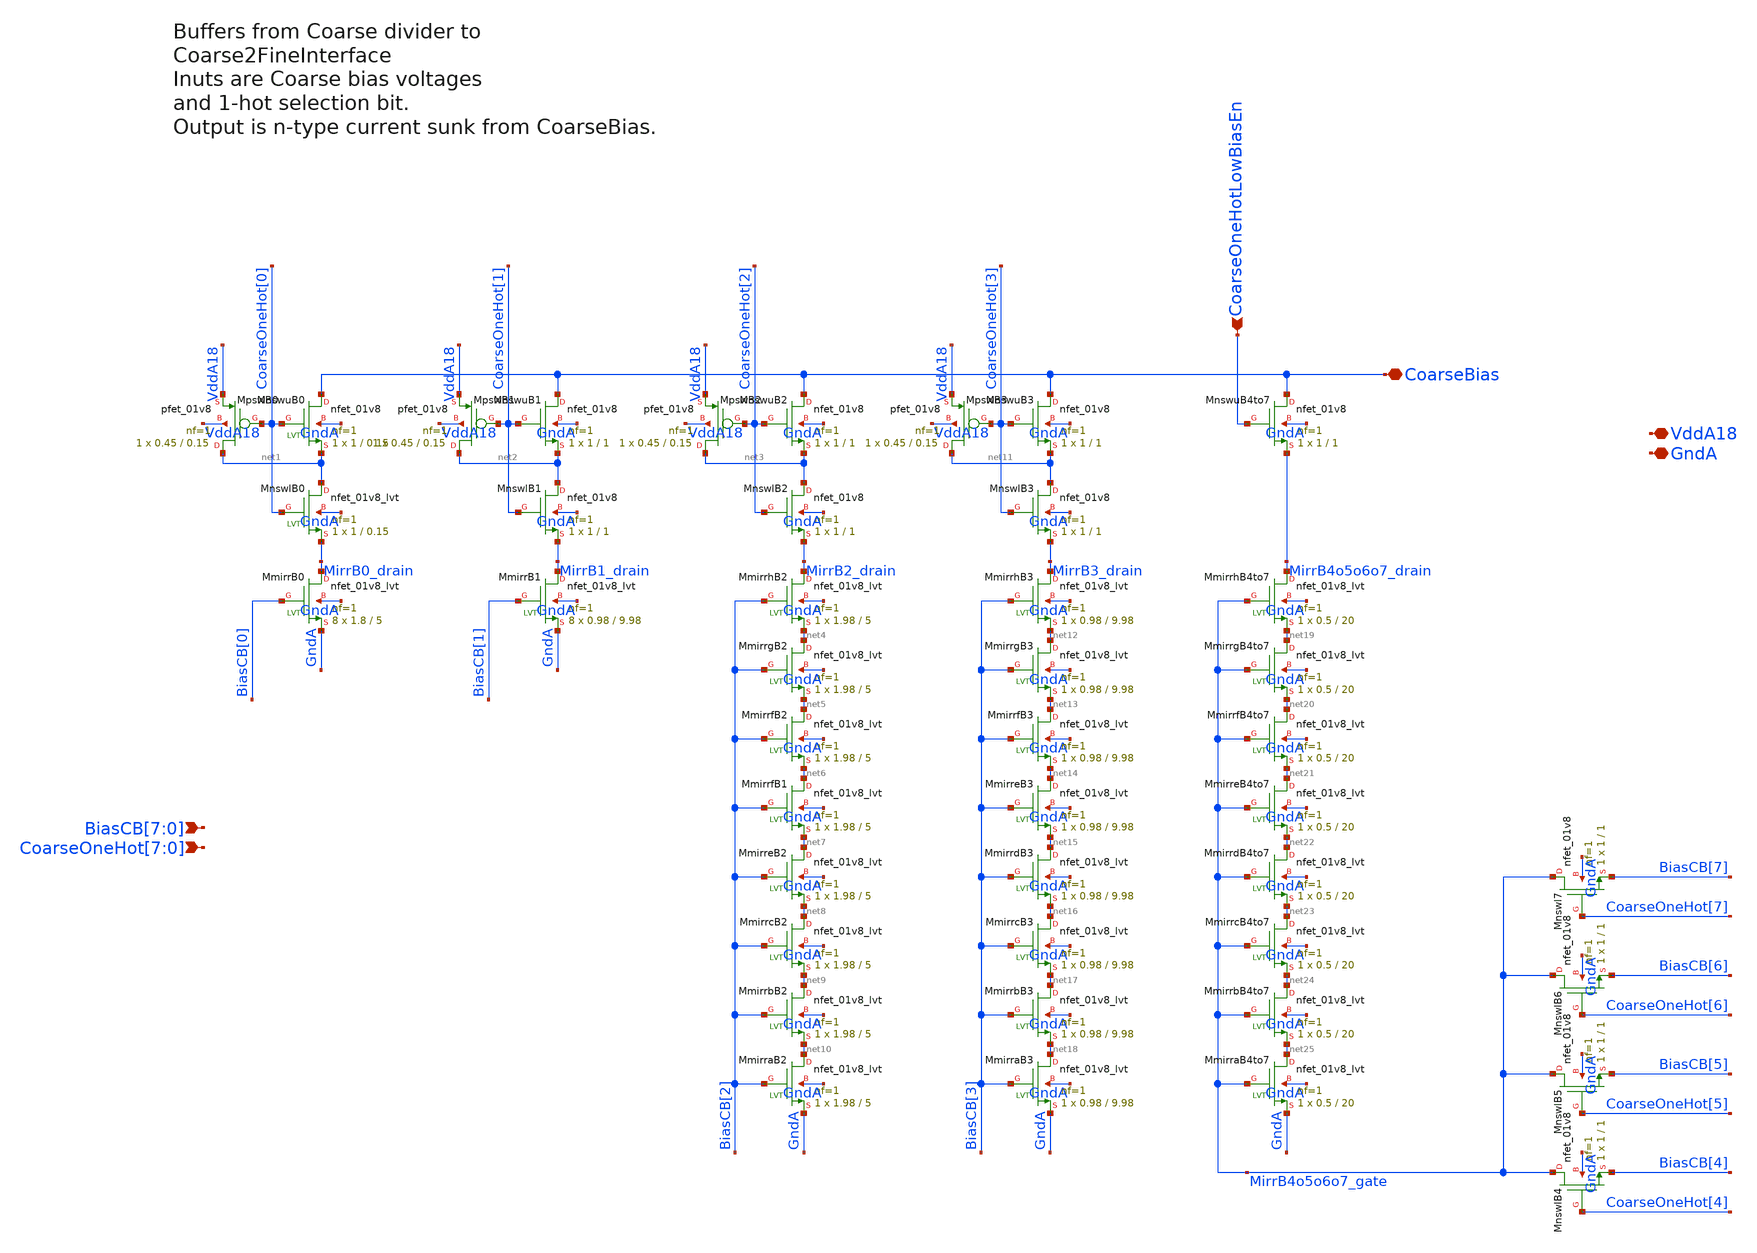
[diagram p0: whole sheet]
** sch_path: analog/klayout/production/final_merge_20260923/testbenches/cace/analog/xschem/BiasCoarseSel8to1.sch
**.subckt BiasCoarseSel8to1
*+ BiasCB[7],BiasCB[6],BiasCB[5],BiasCB[4],BiasCB[3],BiasCB[2],BiasCB[1],BiasCB[0]
*+ CoarseOneHot[7],CoarseOneHot[6],CoarseOneHot[5],CoarseOneHot[4],CoarseOneHot[3],CoarseOneHot[2],CoarseOneHot[1],CoarseOneHot[0] CoarseBias VddA18 GndA CoarseOneHotLowBiasEn
*.ipin BiasCB[7],BiasCB[6],BiasCB[5],BiasCB[4],BiasCB[3],BiasCB[2],BiasCB[1],BiasCB[0]
*.ipin
*+ CoarseOneHot[7],CoarseOneHot[6],CoarseOneHot[5],CoarseOneHot[4],CoarseOneHot[3],CoarseOneHot[2],CoarseOneHot[1],CoarseOneHot[0]
*.iopin CoarseBias
*.iopin VddA18
*.iopin GndA
*.ipin CoarseOneHotLowBiasEn
XMpswB0 net1 CoarseOneHot[0] VddA18 VddA18 sky130_fd_pr__pfet_01v8 L=0.15 W=0.45 nf=1 ad='int((1 + 1)/2) * 0.45 / 1 * 0.29'
+ as='int((1 + 2)/2) * 0.45 / 1 * 0.29' pd='2*int((1 + 1)/2) * (0.45 / 1 + 0.29)' ps='2*int((1 + 2)/2) * (0.45 / 1 + 0.29)'
+ nrd='0.29 / 0.45 ' nrs='0.29 / 0.45 ' sa=0 sb=0 sd=0 mult=1 m=1
XMnswuB0 CoarseBias CoarseOneHot[0] net1 GndA sky130_fd_pr__nfet_01v8 L=0.15 W=1 nf=1 ad='int((1 + 1)/2) * 1 / 1 * 0.29'
+ as='int((1 + 2)/2) * 1 / 1 * 0.29' pd='2*int((1 + 1)/2) * (1 / 1 + 0.29)' ps='2*int((1 + 2)/2) * (1 / 1 + 0.29)'
+ nrd='0.29 / 1 ' nrs='0.29 / 1 ' sa=0 sb=0 sd=0 mult=1 m=1
XMnswlB0 net1 CoarseOneHot[0] MirrB0_drain GndA sky130_fd_pr__nfet_01v8_lvt L=0.15 W=1 nf=1 ad='int((1 + 1)/2) * 1 / 1 * 0.29'
+ as='int((1 + 2)/2) * 1 / 1 * 0.29' pd='2*int((1 + 1)/2) * (1 / 1 + 0.29)' ps='2*int((1 + 2)/2) * (1 / 1 + 0.29)'
+ nrd='0.29 / 1 ' nrs='0.29 / 1 ' sa=0 sb=0 sd=0 mult=1 m=1
XMmirrB0 MirrB0_drain BiasCB[0] GndA GndA sky130_fd_pr__nfet_01v8_lvt L=5 W=1.8 nf=1 ad='int((1 + 1)/2) * 1.8 / 1 * 0.29'
+ as='int((1 + 2)/2) * 1.8 / 1 * 0.29' pd='2*int((1 + 1)/2) * (1.8 / 1 + 0.29)' ps='2*int((1 + 2)/2) * (1.8 / 1 + 0.29)'
+ nrd='0.29 / 1.8 ' nrs='0.29 / 1.8 ' sa=0 sb=0 sd=0 mult=8 m=8
XMpswB1 net2 CoarseOneHot[1] VddA18 VddA18 sky130_fd_pr__pfet_01v8 L=0.15 W=0.45 nf=1 ad='int((1 + 1)/2) * 0.45 / 1 * 0.29'
+ as='int((1 + 2)/2) * 0.45 / 1 * 0.29' pd='2*int((1 + 1)/2) * (0.45 / 1 + 0.29)' ps='2*int((1 + 2)/2) * (0.45 / 1 + 0.29)'
+ nrd='0.29 / 0.45 ' nrs='0.29 / 0.45 ' sa=0 sb=0 sd=0 mult=1 m=1
XMnswuB1 CoarseBias CoarseOneHot[1] net2 GndA sky130_fd_pr__nfet_01v8 L=1 W=1 nf=1 ad='int((1 + 1)/2) * 1 / 1 * 0.29'
+ as='int((1 + 2)/2) * 1 / 1 * 0.29' pd='2*int((1 + 1)/2) * (1 / 1 + 0.29)' ps='2*int((1 + 2)/2) * (1 / 1 + 0.29)'
+ nrd='0.29 / 1 ' nrs='0.29 / 1 ' sa=0 sb=0 sd=0 mult=1 m=1
XMnswlB1 net2 CoarseOneHot[1] MirrB1_drain GndA sky130_fd_pr__nfet_01v8 L=1 W=1 nf=1 ad='int((1 + 1)/2) * 1 / 1 * 0.29'
+ as='int((1 + 2)/2) * 1 / 1 * 0.29' pd='2*int((1 + 1)/2) * (1 / 1 + 0.29)' ps='2*int((1 + 2)/2) * (1 / 1 + 0.29)'
+ nrd='0.29 / 1 ' nrs='0.29 / 1 ' sa=0 sb=0 sd=0 mult=1 m=1
XMmirrB1 MirrB1_drain BiasCB[1] GndA GndA sky130_fd_pr__nfet_01v8_lvt L=9.98 W=0.98 nf=1 ad='int((1 + 1)/2) * 0.98 / 1 * 0.29'
+ as='int((1 + 2)/2) * 0.98 / 1 * 0.29' pd='2*int((1 + 1)/2) * (0.98 / 1 + 0.29)' ps='2*int((1 + 2)/2) * (0.98 / 1 + 0.29)'
+ nrd='0.29 / 0.98 ' nrs='0.29 / 0.98 ' sa=0 sb=0 sd=0 mult=8 m=8
XMpswB2 net3 CoarseOneHot[2] VddA18 VddA18 sky130_fd_pr__pfet_01v8 L=0.15 W=0.45 nf=1 ad='int((1 + 1)/2) * 0.45 / 1 * 0.29'
+ as='int((1 + 2)/2) * 0.45 / 1 * 0.29' pd='2*int((1 + 1)/2) * (0.45 / 1 + 0.29)' ps='2*int((1 + 2)/2) * (0.45 / 1 + 0.29)'
+ nrd='0.29 / 0.45 ' nrs='0.29 / 0.45 ' sa=0 sb=0 sd=0 mult=1 m=1
XMnswuB2 CoarseBias CoarseOneHot[2] net3 GndA sky130_fd_pr__nfet_01v8 L=1 W=1 nf=1 ad='int((1 + 1)/2) * 1 / 1 * 0.29'
+ as='int((1 + 2)/2) * 1 / 1 * 0.29' pd='2*int((1 + 1)/2) * (1 / 1 + 0.29)' ps='2*int((1 + 2)/2) * (1 / 1 + 0.29)'
+ nrd='0.29 / 1 ' nrs='0.29 / 1 ' sa=0 sb=0 sd=0 mult=1 m=1
XMnswlB2 net3 CoarseOneHot[2] MirrB2_drain GndA sky130_fd_pr__nfet_01v8 L=1 W=1 nf=1 ad='int((1 + 1)/2) * 1 / 1 * 0.29'
+ as='int((1 + 2)/2) * 1 / 1 * 0.29' pd='2*int((1 + 1)/2) * (1 / 1 + 0.29)' ps='2*int((1 + 2)/2) * (1 / 1 + 0.29)'
+ nrd='0.29 / 1 ' nrs='0.29 / 1 ' sa=0 sb=0 sd=0 mult=1 m=1
XMmirrhB2 MirrB2_drain BiasCB[2] net4 GndA sky130_fd_pr__nfet_01v8_lvt L=5 W=1.98 nf=1 ad='int((1 + 1)/2) * 1.98 / 1 * 0.29'
+ as='int((1 + 2)/2) * 1.98 / 1 * 0.29' pd='2*int((1 + 1)/2) * (1.98 / 1 + 0.29)' ps='2*int((1 + 2)/2) * (1.98 / 1 + 0.29)'
+ nrd='0.29 / 1.98 ' nrs='0.29 / 1.98 ' sa=0 sb=0 sd=0 mult=1 m=1
XMmirrgB2 net4 BiasCB[2] net5 GndA sky130_fd_pr__nfet_01v8_lvt L=5 W=1.98 nf=1 ad='int((1 + 1)/2) * 1.98 / 1 * 0.29'
+ as='int((1 + 2)/2) * 1.98 / 1 * 0.29' pd='2*int((1 + 1)/2) * (1.98 / 1 + 0.29)' ps='2*int((1 + 2)/2) * (1.98 / 1 + 0.29)'
+ nrd='0.29 / 1.98 ' nrs='0.29 / 1.98 ' sa=0 sb=0 sd=0 mult=1 m=1
XMmirrfB2 net5 BiasCB[2] net6 GndA sky130_fd_pr__nfet_01v8_lvt L=5 W=1.98 nf=1 ad='int((1 + 1)/2) * 1.98 / 1 * 0.29'
+ as='int((1 + 2)/2) * 1.98 / 1 * 0.29' pd='2*int((1 + 1)/2) * (1.98 / 1 + 0.29)' ps='2*int((1 + 2)/2) * (1.98 / 1 + 0.29)'
+ nrd='0.29 / 1.98 ' nrs='0.29 / 1.98 ' sa=0 sb=0 sd=0 mult=1 m=1
XMmirrfB1 net6 BiasCB[2] net7 GndA sky130_fd_pr__nfet_01v8_lvt L=5 W=1.98 nf=1 ad='int((1 + 1)/2) * 1.98 / 1 * 0.29'
+ as='int((1 + 2)/2) * 1.98 / 1 * 0.29' pd='2*int((1 + 1)/2) * (1.98 / 1 + 0.29)' ps='2*int((1 + 2)/2) * (1.98 / 1 + 0.29)'
+ nrd='0.29 / 1.98 ' nrs='0.29 / 1.98 ' sa=0 sb=0 sd=0 mult=1 m=1
XMmirreB2 net7 BiasCB[2] net8 GndA sky130_fd_pr__nfet_01v8_lvt L=5 W=1.98 nf=1 ad='int((1 + 1)/2) * 1.98 / 1 * 0.29'
+ as='int((1 + 2)/2) * 1.98 / 1 * 0.29' pd='2*int((1 + 1)/2) * (1.98 / 1 + 0.29)' ps='2*int((1 + 2)/2) * (1.98 / 1 + 0.29)'
+ nrd='0.29 / 1.98 ' nrs='0.29 / 1.98 ' sa=0 sb=0 sd=0 mult=1 m=1
XMmirrcB2 net8 BiasCB[2] net9 GndA sky130_fd_pr__nfet_01v8_lvt L=5 W=1.98 nf=1 ad='int((1 + 1)/2) * 1.98 / 1 * 0.29'
+ as='int((1 + 2)/2) * 1.98 / 1 * 0.29' pd='2*int((1 + 1)/2) * (1.98 / 1 + 0.29)' ps='2*int((1 + 2)/2) * (1.98 / 1 + 0.29)'
+ nrd='0.29 / 1.98 ' nrs='0.29 / 1.98 ' sa=0 sb=0 sd=0 mult=1 m=1
XMmirrbB2 net9 BiasCB[2] net10 GndA sky130_fd_pr__nfet_01v8_lvt L=5 W=1.98 nf=1 ad='int((1 + 1)/2) * 1.98 / 1 * 0.29'
+ as='int((1 + 2)/2) * 1.98 / 1 * 0.29' pd='2*int((1 + 1)/2) * (1.98 / 1 + 0.29)' ps='2*int((1 + 2)/2) * (1.98 / 1 + 0.29)'
+ nrd='0.29 / 1.98 ' nrs='0.29 / 1.98 ' sa=0 sb=0 sd=0 mult=1 m=1
XMmirraB2 net10 BiasCB[2] GndA GndA sky130_fd_pr__nfet_01v8_lvt L=5 W=1.98 nf=1 ad='int((1 + 1)/2) * 1.98 / 1 * 0.29'
+ as='int((1 + 2)/2) * 1.98 / 1 * 0.29' pd='2*int((1 + 1)/2) * (1.98 / 1 + 0.29)' ps='2*int((1 + 2)/2) * (1.98 / 1 + 0.29)'
+ nrd='0.29 / 1.98 ' nrs='0.29 / 1.98 ' sa=0 sb=0 sd=0 mult=1 m=1
XMpswB3 net11 CoarseOneHot[3] VddA18 VddA18 sky130_fd_pr__pfet_01v8 L=0.15 W=0.45 nf=1 ad='int((1 + 1)/2) * 0.45 / 1 * 0.29'
+ as='int((1 + 2)/2) * 0.45 / 1 * 0.29' pd='2*int((1 + 1)/2) * (0.45 / 1 + 0.29)' ps='2*int((1 + 2)/2) * (0.45 / 1 + 0.29)'
+ nrd='0.29 / 0.45 ' nrs='0.29 / 0.45 ' sa=0 sb=0 sd=0 mult=1 m=1
XMnswuB3 CoarseBias CoarseOneHot[3] net11 GndA sky130_fd_pr__nfet_01v8 L=1 W=1 nf=1 ad='int((1 + 1)/2) * 1 / 1 * 0.29'
+ as='int((1 + 2)/2) * 1 / 1 * 0.29' pd='2*int((1 + 1)/2) * (1 / 1 + 0.29)' ps='2*int((1 + 2)/2) * (1 / 1 + 0.29)'
+ nrd='0.29 / 1 ' nrs='0.29 / 1 ' sa=0 sb=0 sd=0 mult=1 m=1
XMnswlB3 net11 CoarseOneHot[3] MirrB3_drain GndA sky130_fd_pr__nfet_01v8 L=1 W=1 nf=1 ad='int((1 + 1)/2) * 1 / 1 * 0.29'
+ as='int((1 + 2)/2) * 1 / 1 * 0.29' pd='2*int((1 + 1)/2) * (1 / 1 + 0.29)' ps='2*int((1 + 2)/2) * (1 / 1 + 0.29)'
+ nrd='0.29 / 1 ' nrs='0.29 / 1 ' sa=0 sb=0 sd=0 mult=1 m=1
XMmirrhB3 MirrB3_drain BiasCB[3] net12 GndA sky130_fd_pr__nfet_01v8_lvt L=9.98 W=0.98 nf=1 ad='int((1 + 1)/2) * 0.98 / 1 * 0.29'
+ as='int((1 + 2)/2) * 0.98 / 1 * 0.29' pd='2*int((1 + 1)/2) * (0.98 / 1 + 0.29)' ps='2*int((1 + 2)/2) * (0.98 / 1 + 0.29)'
+ nrd='0.29 / 0.98 ' nrs='0.29 / 0.98 ' sa=0 sb=0 sd=0 mult=1 m=1
XMmirrgB3 net12 BiasCB[3] net13 GndA sky130_fd_pr__nfet_01v8_lvt L=9.98 W=0.98 nf=1 ad='int((1 + 1)/2) * 0.98 / 1 * 0.29'
+ as='int((1 + 2)/2) * 0.98 / 1 * 0.29' pd='2*int((1 + 1)/2) * (0.98 / 1 + 0.29)' ps='2*int((1 + 2)/2) * (0.98 / 1 + 0.29)'
+ nrd='0.29 / 0.98 ' nrs='0.29 / 0.98 ' sa=0 sb=0 sd=0 mult=1 m=1
XMmirrfB3 net13 BiasCB[3] net14 GndA sky130_fd_pr__nfet_01v8_lvt L=9.98 W=0.98 nf=1 ad='int((1 + 1)/2) * 0.98 / 1 * 0.29'
+ as='int((1 + 2)/2) * 0.98 / 1 * 0.29' pd='2*int((1 + 1)/2) * (0.98 / 1 + 0.29)' ps='2*int((1 + 2)/2) * (0.98 / 1 + 0.29)'
+ nrd='0.29 / 0.98 ' nrs='0.29 / 0.98 ' sa=0 sb=0 sd=0 mult=1 m=1
XMmirreB3 net14 BiasCB[3] net15 GndA sky130_fd_pr__nfet_01v8_lvt L=9.98 W=0.98 nf=1 ad='int((1 + 1)/2) * 0.98 / 1 * 0.29'
+ as='int((1 + 2)/2) * 0.98 / 1 * 0.29' pd='2*int((1 + 1)/2) * (0.98 / 1 + 0.29)' ps='2*int((1 + 2)/2) * (0.98 / 1 + 0.29)'
+ nrd='0.29 / 0.98 ' nrs='0.29 / 0.98 ' sa=0 sb=0 sd=0 mult=1 m=1
XMmirrdB3 net15 BiasCB[3] net16 GndA sky130_fd_pr__nfet_01v8_lvt L=9.98 W=0.98 nf=1 ad='int((1 + 1)/2) * 0.98 / 1 * 0.29'
+ as='int((1 + 2)/2) * 0.98 / 1 * 0.29' pd='2*int((1 + 1)/2) * (0.98 / 1 + 0.29)' ps='2*int((1 + 2)/2) * (0.98 / 1 + 0.29)'
+ nrd='0.29 / 0.98 ' nrs='0.29 / 0.98 ' sa=0 sb=0 sd=0 mult=1 m=1
XMmirrcB3 net16 BiasCB[3] net17 GndA sky130_fd_pr__nfet_01v8_lvt L=9.98 W=0.98 nf=1 ad='int((1 + 1)/2) * 0.98 / 1 * 0.29'
+ as='int((1 + 2)/2) * 0.98 / 1 * 0.29' pd='2*int((1 + 1)/2) * (0.98 / 1 + 0.29)' ps='2*int((1 + 2)/2) * (0.98 / 1 + 0.29)'
+ nrd='0.29 / 0.98 ' nrs='0.29 / 0.98 ' sa=0 sb=0 sd=0 mult=1 m=1
XMmirrbB3 net17 BiasCB[3] net18 GndA sky130_fd_pr__nfet_01v8_lvt L=9.98 W=0.98 nf=1 ad='int((1 + 1)/2) * 0.98 / 1 * 0.29'
+ as='int((1 + 2)/2) * 0.98 / 1 * 0.29' pd='2*int((1 + 1)/2) * (0.98 / 1 + 0.29)' ps='2*int((1 + 2)/2) * (0.98 / 1 + 0.29)'
+ nrd='0.29 / 0.98 ' nrs='0.29 / 0.98 ' sa=0 sb=0 sd=0 mult=1 m=1
XMmirraB3 net18 BiasCB[3] GndA GndA sky130_fd_pr__nfet_01v8_lvt L=9.98 W=0.98 nf=1 ad='int((1 + 1)/2) * 0.98 / 1 * 0.29'
+ as='int((1 + 2)/2) * 0.98 / 1 * 0.29' pd='2*int((1 + 1)/2) * (0.98 / 1 + 0.29)' ps='2*int((1 + 2)/2) * (0.98 / 1 + 0.29)'
+ nrd='0.29 / 0.98 ' nrs='0.29 / 0.98 ' sa=0 sb=0 sd=0 mult=1 m=1
XMnswuB4to7 CoarseBias CoarseOneHotLowBiasEn MirrB4o5o6o7_drain GndA sky130_fd_pr__nfet_01v8 L=1 W=1
+ nf=1 ad='int((1 + 1)/2) * 1 / 1 * 0.29' as='int((1 + 2)/2) * 1 / 1 * 0.29' pd='2*int((1 + 1)/2) * (1 / 1 + 0.29)'
+ ps='2*int((1 + 2)/2) * (1 / 1 + 0.29)' nrd='0.29 / 1 ' nrs='0.29 / 1 ' sa=0 sb=0 sd=0 mult=1 m=1
XMmirrhB4to7 MirrB4o5o6o7_drain MirrB4o5o6o7_gate net19 GndA sky130_fd_pr__nfet_01v8_lvt L=20 W=0.5 nf=1
+ ad='int((1 + 1)/2) * 0.5 / 1 * 0.29' as='int((1 + 2)/2) * 0.5 / 1 * 0.29' pd='2*int((1 + 1)/2) * (0.5 / 1 + 0.29)'
+ ps='2*int((1 + 2)/2) * (0.5 / 1 + 0.29)' nrd='0.29 / 0.5 ' nrs='0.29 / 0.5 ' sa=0 sb=0 sd=0 mult=1 m=1
XMmirraB4to7 net25 MirrB4o5o6o7_gate GndA GndA sky130_fd_pr__nfet_01v8_lvt L=20 W=0.5 nf=1 ad='int((1 + 1)/2) * 0.5 / 1 * 0.29'
+ as='int((1 + 2)/2) * 0.5 / 1 * 0.29' pd='2*int((1 + 1)/2) * (0.5 / 1 + 0.29)' ps='2*int((1 + 2)/2) * (0.5 / 1 + 0.29)'
+ nrd='0.29 / 0.5 ' nrs='0.29 / 0.5 ' sa=0 sb=0 sd=0 mult=1 m=1
XMmirrbB4to7 net24 MirrB4o5o6o7_gate net25 GndA sky130_fd_pr__nfet_01v8_lvt L=20 W=0.5 nf=1 ad='int((1 + 1)/2) * 0.5 / 1 * 0.29'
+ as='int((1 + 2)/2) * 0.5 / 1 * 0.29' pd='2*int((1 + 1)/2) * (0.5 / 1 + 0.29)' ps='2*int((1 + 2)/2) * (0.5 / 1 + 0.29)'
+ nrd='0.29 / 0.5 ' nrs='0.29 / 0.5 ' sa=0 sb=0 sd=0 mult=1 m=1
XMmirrcB4to7 net23 MirrB4o5o6o7_gate net24 GndA sky130_fd_pr__nfet_01v8_lvt L=20 W=0.5 nf=1 ad='int((1 + 1)/2) * 0.5 / 1 * 0.29'
+ as='int((1 + 2)/2) * 0.5 / 1 * 0.29' pd='2*int((1 + 1)/2) * (0.5 / 1 + 0.29)' ps='2*int((1 + 2)/2) * (0.5 / 1 + 0.29)'
+ nrd='0.29 / 0.5 ' nrs='0.29 / 0.5 ' sa=0 sb=0 sd=0 mult=1 m=1
XMmirrdB4to7 net22 MirrB4o5o6o7_gate net23 GndA sky130_fd_pr__nfet_01v8_lvt L=20 W=0.5 nf=1 ad='int((1 + 1)/2) * 0.5 / 1 * 0.29'
+ as='int((1 + 2)/2) * 0.5 / 1 * 0.29' pd='2*int((1 + 1)/2) * (0.5 / 1 + 0.29)' ps='2*int((1 + 2)/2) * (0.5 / 1 + 0.29)'
+ nrd='0.29 / 0.5 ' nrs='0.29 / 0.5 ' sa=0 sb=0 sd=0 mult=1 m=1
XMmirreB4to7 net21 MirrB4o5o6o7_gate net22 GndA sky130_fd_pr__nfet_01v8_lvt L=20 W=0.5 nf=1 ad='int((1 + 1)/2) * 0.5 / 1 * 0.29'
+ as='int((1 + 2)/2) * 0.5 / 1 * 0.29' pd='2*int((1 + 1)/2) * (0.5 / 1 + 0.29)' ps='2*int((1 + 2)/2) * (0.5 / 1 + 0.29)'
+ nrd='0.29 / 0.5 ' nrs='0.29 / 0.5 ' sa=0 sb=0 sd=0 mult=1 m=1
XMmirrfB4to7 net20 MirrB4o5o6o7_gate net21 GndA sky130_fd_pr__nfet_01v8_lvt L=20 W=0.5 nf=1 ad='int((1 + 1)/2) * 0.5 / 1 * 0.29'
+ as='int((1 + 2)/2) * 0.5 / 1 * 0.29' pd='2*int((1 + 1)/2) * (0.5 / 1 + 0.29)' ps='2*int((1 + 2)/2) * (0.5 / 1 + 0.29)'
+ nrd='0.29 / 0.5 ' nrs='0.29 / 0.5 ' sa=0 sb=0 sd=0 mult=1 m=1
XMmirrgB4to7 net19 MirrB4o5o6o7_gate net20 GndA sky130_fd_pr__nfet_01v8_lvt L=20 W=0.5 nf=1 ad='int((1 + 1)/2) * 0.5 / 1 * 0.29'
+ as='int((1 + 2)/2) * 0.5 / 1 * 0.29' pd='2*int((1 + 1)/2) * (0.5 / 1 + 0.29)' ps='2*int((1 + 2)/2) * (0.5 / 1 + 0.29)'
+ nrd='0.29 / 0.5 ' nrs='0.29 / 0.5 ' sa=0 sb=0 sd=0 mult=1 m=1
XMnswl7 MirrB4o5o6o7_gate CoarseOneHot[7] BiasCB[7] GndA sky130_fd_pr__nfet_01v8 L=1 W=1 nf=1 ad='int((1 + 1)/2) * 1 / 1 * 0.29'
+ as='int((1 + 2)/2) * 1 / 1 * 0.29' pd='2*int((1 + 1)/2) * (1 / 1 + 0.29)' ps='2*int((1 + 2)/2) * (1 / 1 + 0.29)'
+ nrd='0.29 / 1 ' nrs='0.29 / 1 ' sa=0 sb=0 sd=0 mult=1 m=1
XMnswlB6 MirrB4o5o6o7_gate CoarseOneHot[6] BiasCB[6] GndA sky130_fd_pr__nfet_01v8 L=1 W=1 nf=1 ad='int((1 + 1)/2) * 1 / 1 * 0.29'
+ as='int((1 + 2)/2) * 1 / 1 * 0.29' pd='2*int((1 + 1)/2) * (1 / 1 + 0.29)' ps='2*int((1 + 2)/2) * (1 / 1 + 0.29)'
+ nrd='0.29 / 1 ' nrs='0.29 / 1 ' sa=0 sb=0 sd=0 mult=1 m=1
XMnswlB5 MirrB4o5o6o7_gate CoarseOneHot[5] BiasCB[5] GndA sky130_fd_pr__nfet_01v8 L=1 W=1 nf=1 ad='int((1 + 1)/2) * 1 / 1 * 0.29'
+ as='int((1 + 2)/2) * 1 / 1 * 0.29' pd='2*int((1 + 1)/2) * (1 / 1 + 0.29)' ps='2*int((1 + 2)/2) * (1 / 1 + 0.29)'
+ nrd='0.29 / 1 ' nrs='0.29 / 1 ' sa=0 sb=0 sd=0 mult=1 m=1
XMnswlB4 MirrB4o5o6o7_gate CoarseOneHot[4] BiasCB[4] GndA sky130_fd_pr__nfet_01v8 L=1 W=1 nf=1 ad='int((1 + 1)/2) * 1 / 1 * 0.29'
+ as='int((1 + 2)/2) * 1 / 1 * 0.29' pd='2*int((1 + 1)/2) * (1 / 1 + 0.29)' ps='2*int((1 + 2)/2) * (1 / 1 + 0.29)'
+ nrd='0.29 / 1 ' nrs='0.29 / 1 ' sa=0 sb=0 sd=0 mult=1 m=1
**.ends
.end
